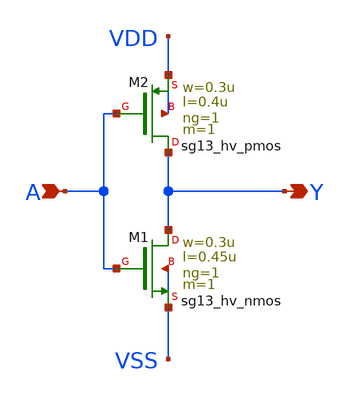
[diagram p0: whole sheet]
** sch_path: FLDO/design_data/xschem/shifter_down_invert.sch
**.subckt shifter_down_invert Y A
*.opin Y
*.ipin A
XM1 Y A VSS VSS sg13_hv_nmos w=0.3u l=0.45u ng=1 m=1 mm_ok=1
XM2 Y A VDD VDD sg13_hv_pmos w=0.3u l=0.4u ng=1 m=1 mm_ok=1
**.ends
.end
